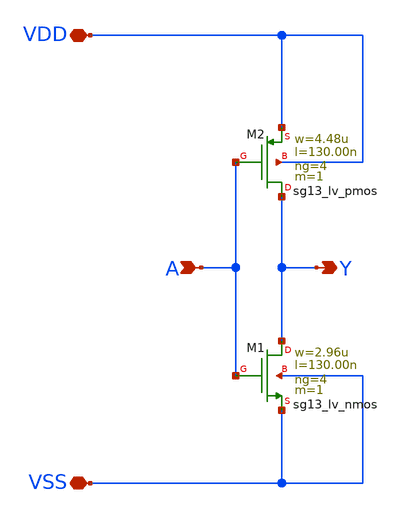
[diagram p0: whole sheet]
** sch_path: ihp-sg13g2/libs.tech/xschem/sg13g2_stdcells/sg13g2_inv_4.sch
* Copyright 2023 IHP PDK Authors
* Licensed under the Apache License, Version 2.0 (the "License");
* you may not use this file except in compliance with the License.
* You may obtain a copy of the License at
* https://www.apache.org/licenses/LICENSE-2.0
* Unless required by applicable law or agreed to in writing, software
* distributed under the License is distributed on an "AS IS" BASIS,
* WITHOUT WARRANTIES OR CONDITIONS OF ANY KIND, either express or implied.
* See the License for the specific language governing permissions and
* limitations under the License.
**.subckt sg13g2_inv_4 A Y VDD VSS
*.ipin A
*.opin Y
*.iopin VDD
*.iopin VSS
XM1 Y A VSS VSS sg13_lv_nmos w=2.96u l=130.00n ng=4 m=1 mm_ok=1
XM2 Y A VDD VDD sg13_lv_pmos w=4.48u l=130.00n ng=4 m=1 mm_ok=1
**.ends
.end
